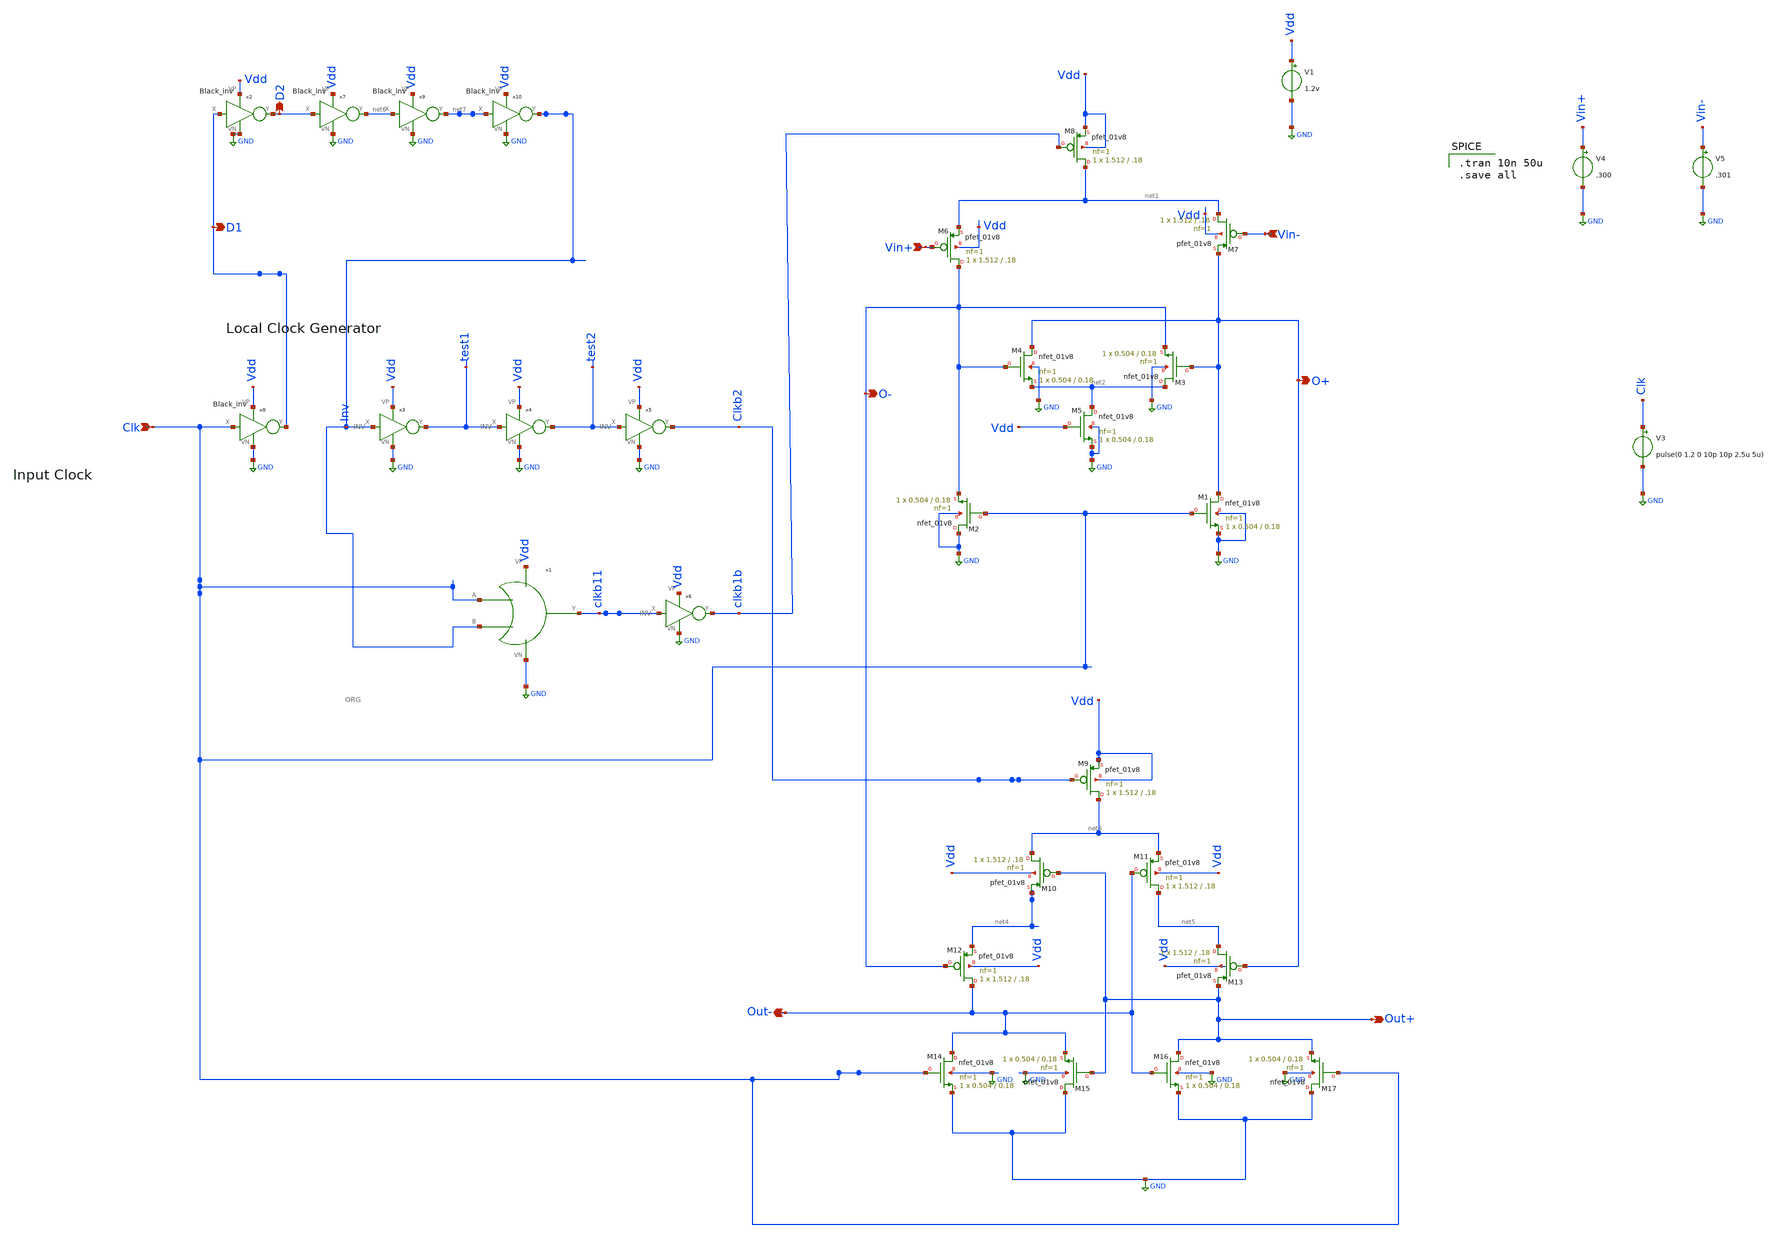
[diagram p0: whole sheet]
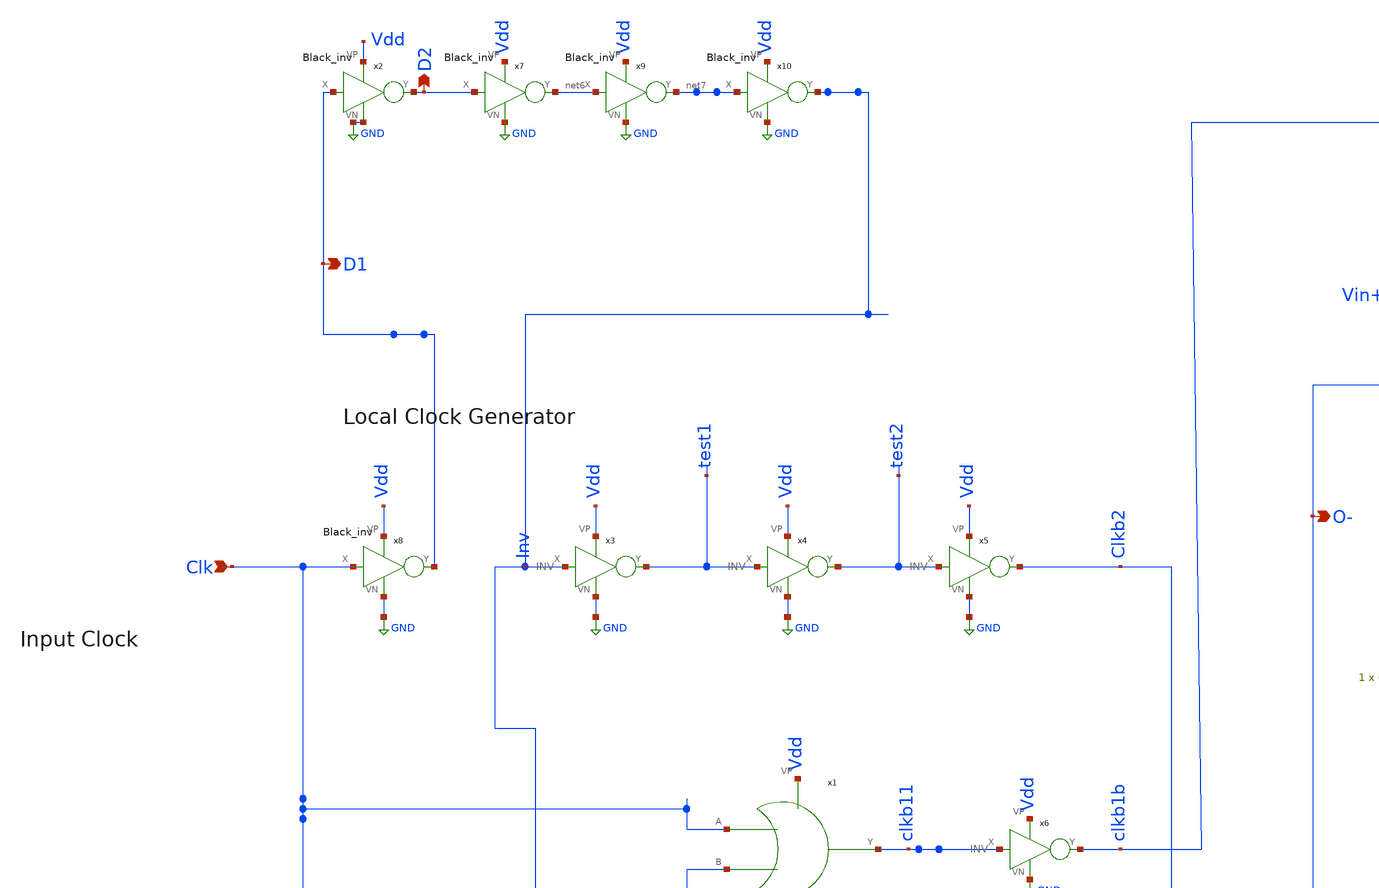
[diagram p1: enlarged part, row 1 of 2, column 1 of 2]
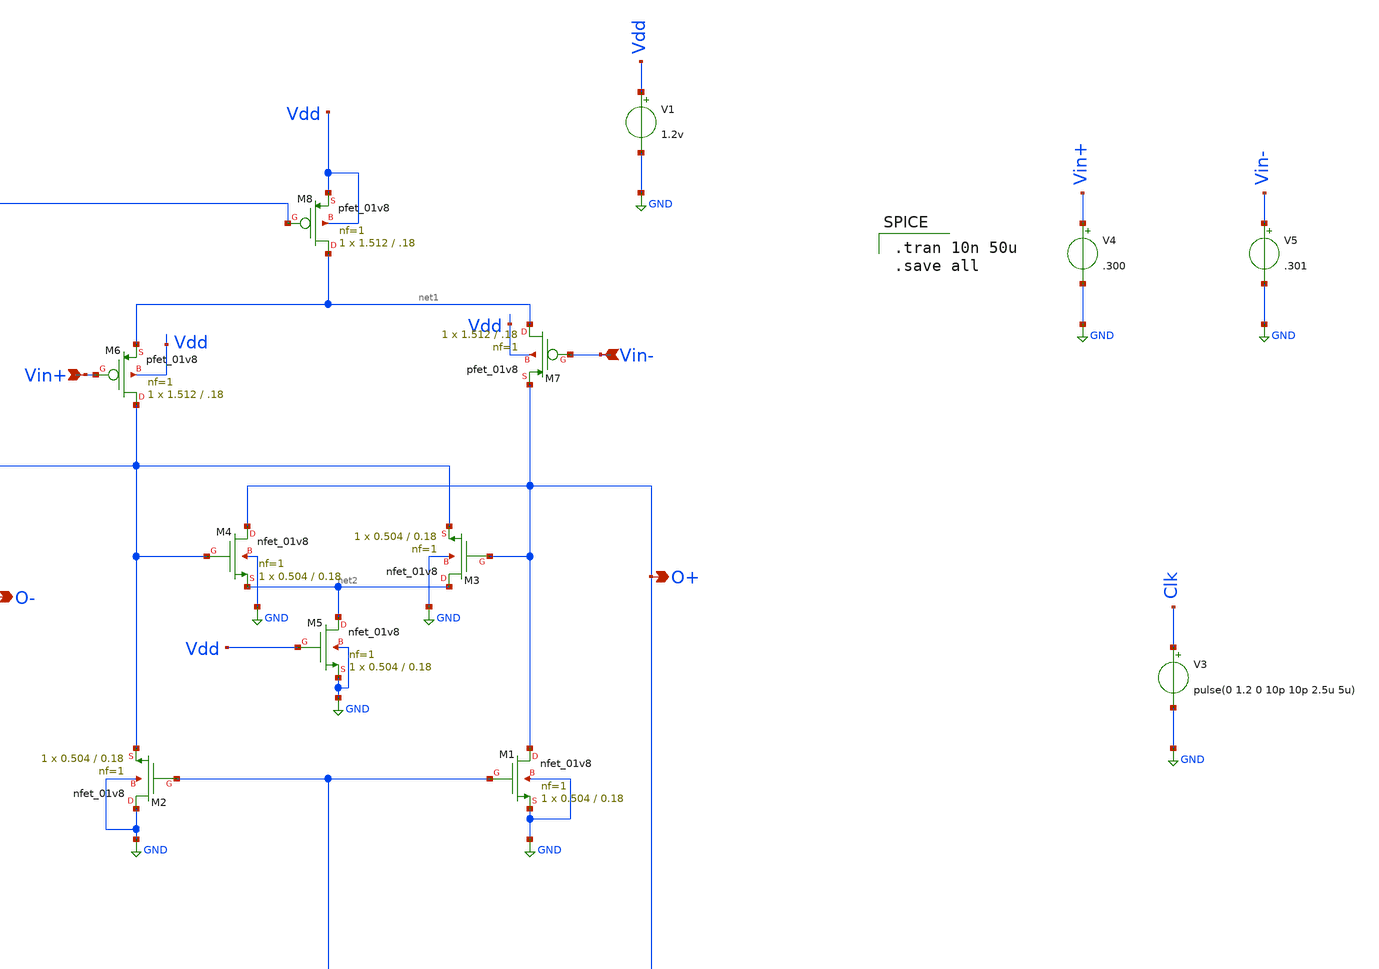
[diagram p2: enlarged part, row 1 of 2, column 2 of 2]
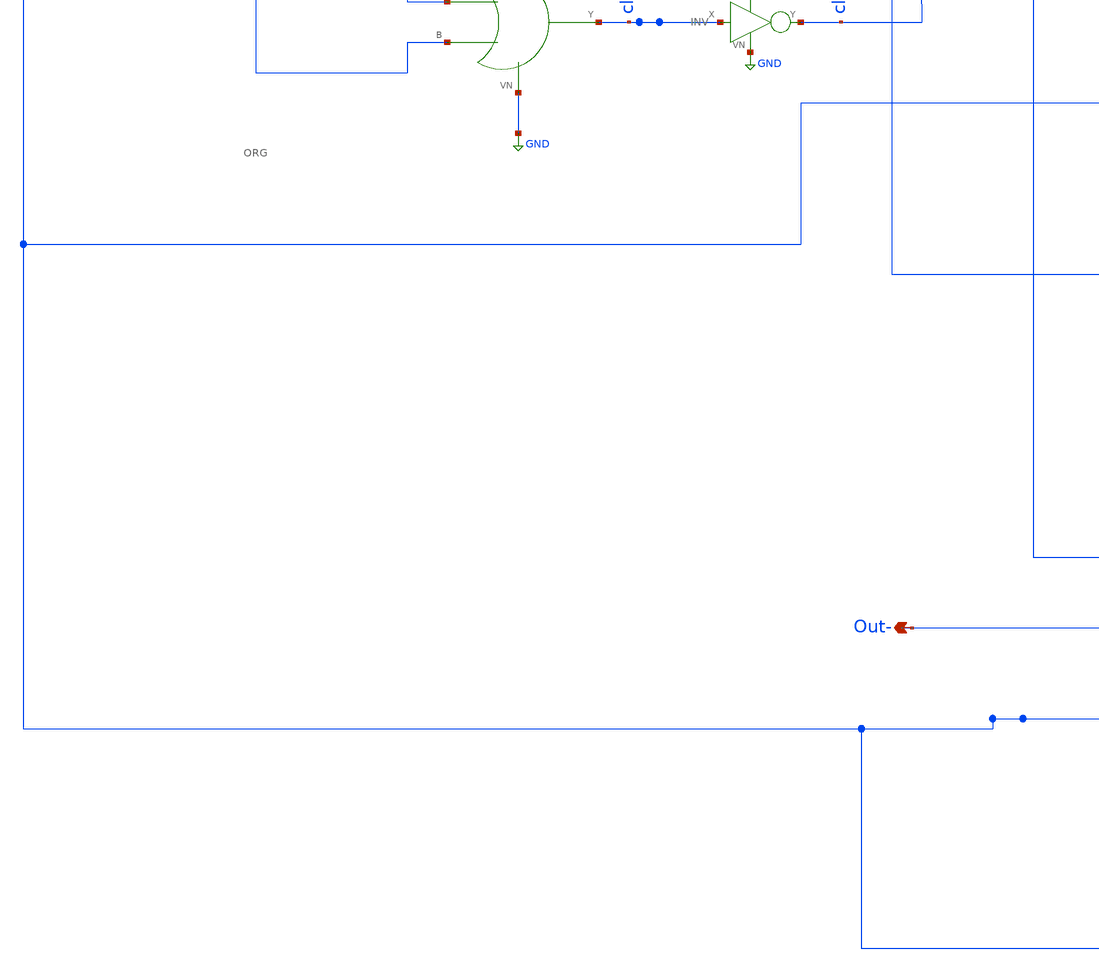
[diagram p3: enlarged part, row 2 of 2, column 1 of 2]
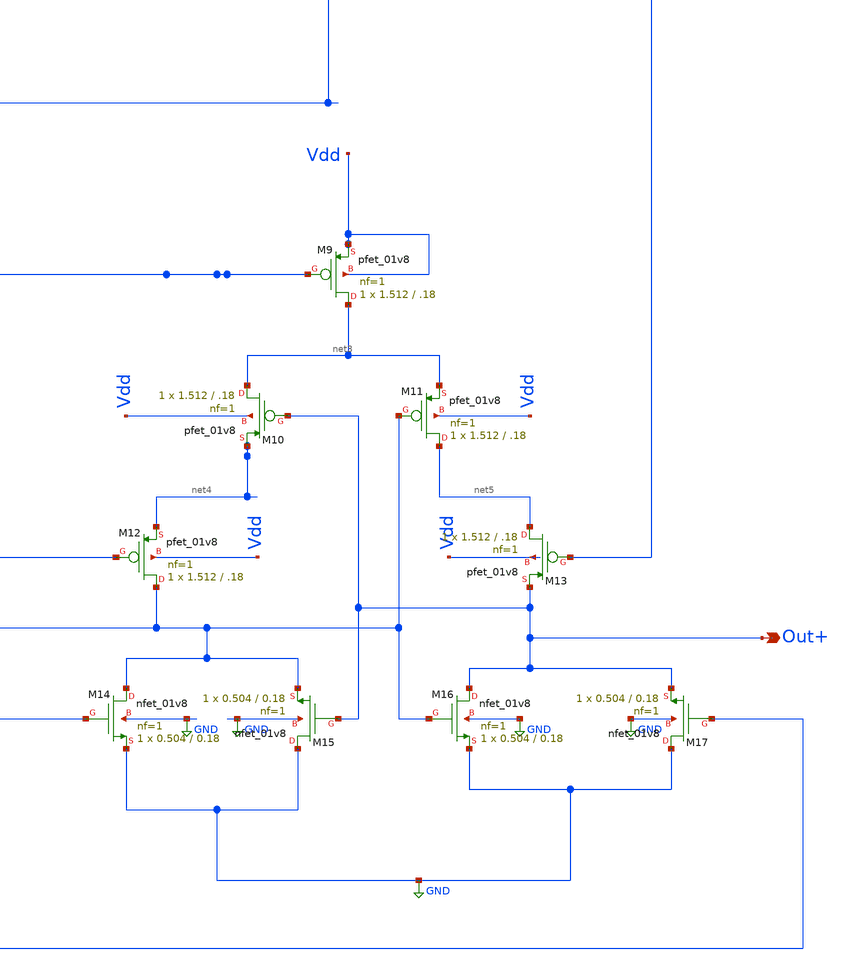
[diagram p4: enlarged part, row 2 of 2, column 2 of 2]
** sch_path: Blocks/Comparator/Comparator.sch
**.subckt Comparator Vin+ Vin- Clk Out+ Out- D2 D1 O- O+
*.ipin Vin+
*.ipin Vin-
*.ipin Clk
*.opin Out+
*.opin Out-
*.opin D2
*.opin D1
*.opin O-
*.opin O+
XM8 net1 clkb1b Vdd Vdd sky130_fd_pr__pfet_01v8 L=.18 W=1.512 nf=1 ad='int((nf+1)/2) * W/nf * 0.29' as='int((nf+2)/2) * W/nf * 0.29'
+ pd='2*int((nf+1)/2) * (W/nf + 0.29)' ps='2*int((nf+2)/2) * (W/nf + 0.29)' nrd='0.29 / W' nrs='0.29 / W'
+ sa=0 sb=0 sd=0 mult=1 m=1
x1 Inv Clk clkb11 Vdd GND ORG
x3 Inv test1 Vdd GND INV
x4 test1 test2 Vdd GND INV
x5 test2 Clkb2 Vdd GND INV
x6 clkb11 clkb1b Vdd GND INV
XM4 O+ O- net2 GND sky130_fd_pr__nfet_01v8 L=0.18 W=0.504 nf=1 ad='int((nf+1)/2) * W/nf * 0.29' as='int((nf+2)/2) * W/nf * 0.29'
+ pd='2*int((nf+1)/2) * (W/nf + 0.29)' ps='2*int((nf+2)/2) * (W/nf + 0.29)' nrd='0.29 / W' nrs='0.29 / W'
+ sa=0 sb=0 sd=0 mult=1 m=1
XM6 O- Vin+ net1 Vdd sky130_fd_pr__pfet_01v8 L=.18 W=1.512 nf=1 ad='int((nf+1)/2) * W/nf * 0.29' as='int((nf+2)/2) * W/nf * 0.29'
+ pd='2*int((nf+1)/2) * (W/nf + 0.29)' ps='2*int((nf+2)/2) * (W/nf + 0.29)' nrd='0.29 / W' nrs='0.29 / W'
+ sa=0 sb=0 sd=0 mult=1 m=1
XM7 net1 Vin- O+ Vdd sky130_fd_pr__pfet_01v8 L=.18 W=1.512 nf=1 ad='int((nf+1)/2) * W/nf * 0.29' as='int((nf+2)/2) * W/nf * 0.29'
+ pd='2*int((nf+1)/2) * (W/nf + 0.29)' ps='2*int((nf+2)/2) * (W/nf + 0.29)' nrd='0.29 / W' nrs='0.29 / W'
+ sa=0 sb=0 sd=0 mult=1 m=1
XM3 net2 O+ O- GND sky130_fd_pr__nfet_01v8 L=0.18 W=0.504 nf=1 ad='int((nf+1)/2) * W/nf * 0.29' as='int((nf+2)/2) * W/nf * 0.29'
+ pd='2*int((nf+1)/2) * (W/nf + 0.29)' ps='2*int((nf+2)/2) * (W/nf + 0.29)' nrd='0.29 / W' nrs='0.29 / W'
+ sa=0 sb=0 sd=0 mult=1 m=1
XM5 net2 Vdd GND GND sky130_fd_pr__nfet_01v8 L=0.18 W=0.504 nf=1 ad='int((nf+1)/2) * W/nf * 0.29' as='int((nf+2)/2) * W/nf * 0.29'
+ pd='2*int((nf+1)/2) * (W/nf + 0.29)' ps='2*int((nf+2)/2) * (W/nf + 0.29)' nrd='0.29 / W' nrs='0.29 / W'
+ sa=0 sb=0 sd=0 mult=1 m=1
XM2 GND Clk O- GND sky130_fd_pr__nfet_01v8 L=0.18 W=0.504 nf=1 ad='int((nf+1)/2) * W/nf * 0.29' as='int((nf+2)/2) * W/nf * 0.29'
+ pd='2*int((nf+1)/2) * (W/nf + 0.29)' ps='2*int((nf+2)/2) * (W/nf + 0.29)' nrd='0.29 / W' nrs='0.29 / W'
+ sa=0 sb=0 sd=0 mult=1 m=1
XM1 O+ Clk GND GND sky130_fd_pr__nfet_01v8 L=0.18 W=0.504 nf=1 ad='int((nf+1)/2) * W/nf * 0.29' as='int((nf+2)/2) * W/nf * 0.29'
+ pd='2*int((nf+1)/2) * (W/nf + 0.29)' ps='2*int((nf+2)/2) * (W/nf + 0.29)' nrd='0.29 / W' nrs='0.29 / W'
+ sa=0 sb=0 sd=0 mult=1 m=1
XM14 Out- Clk GND GND sky130_fd_pr__nfet_01v8 L=0.18 W=0.504 nf=1 ad='int((nf+1)/2) * W/nf * 0.29' as='int((nf+2)/2) * W/nf * 0.29'
+ pd='2*int((nf+1)/2) * (W/nf + 0.29)' ps='2*int((nf+2)/2) * (W/nf + 0.29)' nrd='0.29 / W' nrs='0.29 / W'
+ sa=0 sb=0 sd=0 mult=1 m=1
XM15 GND Out+ Out- GND sky130_fd_pr__nfet_01v8 L=0.18 W=0.504 nf=1 ad='int((nf+1)/2) * W/nf * 0.29' as='int((nf+2)/2) * W/nf * 0.29'
+ pd='2*int((nf+1)/2) * (W/nf + 0.29)' ps='2*int((nf+2)/2) * (W/nf + 0.29)' nrd='0.29 / W' nrs='0.29 / W'
+ sa=0 sb=0 sd=0 mult=1 m=1
XM16 Out+ Out- GND GND sky130_fd_pr__nfet_01v8 L=0.18 W=0.504 nf=1 ad='int((nf+1)/2) * W/nf * 0.29' as='int((nf+2)/2) * W/nf * 0.29'
+ pd='2*int((nf+1)/2) * (W/nf + 0.29)' ps='2*int((nf+2)/2) * (W/nf + 0.29)' nrd='0.29 / W' nrs='0.29 / W'
+ sa=0 sb=0 sd=0 mult=1 m=1
XM17 GND Clk Out+ GND sky130_fd_pr__nfet_01v8 L=0.18 W=0.504 nf=1 ad='int((nf+1)/2) * W/nf * 0.29' as='int((nf+2)/2) * W/nf * 0.29'
+ pd='2*int((nf+1)/2) * (W/nf + 0.29)' ps='2*int((nf+2)/2) * (W/nf + 0.29)' nrd='0.29 / W' nrs='0.29 / W'
+ sa=0 sb=0 sd=0 mult=1 m=1
XM9 net3 Clkb2 Vdd Vdd sky130_fd_pr__pfet_01v8 L=.18 W=1.512 nf=1 ad='int((nf+1)/2) * W/nf * 0.29' as='int((nf+2)/2) * W/nf * 0.29'
+ pd='2*int((nf+1)/2) * (W/nf + 0.29)' ps='2*int((nf+2)/2) * (W/nf + 0.29)' nrd='0.29 / W' nrs='0.29 / W'
+ sa=0 sb=0 sd=0 mult=1 m=1
XM10 net3 Out+ net4 Vdd sky130_fd_pr__pfet_01v8 L=.18 W=1.512 nf=1 ad='int((nf+1)/2) * W/nf * 0.29' as='int((nf+2)/2) * W/nf * 0.29'
+ pd='2*int((nf+1)/2) * (W/nf + 0.29)' ps='2*int((nf+2)/2) * (W/nf + 0.29)' nrd='0.29 / W' nrs='0.29 / W'
+ sa=0 sb=0 sd=0 mult=1 m=1
XM11 net5 Out- net3 Vdd sky130_fd_pr__pfet_01v8 L=.18 W=1.512 nf=1 ad='int((nf+1)/2) * W/nf * 0.29' as='int((nf+2)/2) * W/nf * 0.29'
+ pd='2*int((nf+1)/2) * (W/nf + 0.29)' ps='2*int((nf+2)/2) * (W/nf + 0.29)' nrd='0.29 / W' nrs='0.29 / W'
+ sa=0 sb=0 sd=0 mult=1 m=1
XM13 net5 O+ Out+ Vdd sky130_fd_pr__pfet_01v8 L=.18 W=1.512 nf=1 ad='int((nf+1)/2) * W/nf * 0.29' as='int((nf+2)/2) * W/nf * 0.29'
+ pd='2*int((nf+1)/2) * (W/nf + 0.29)' ps='2*int((nf+2)/2) * (W/nf + 0.29)' nrd='0.29 / W' nrs='0.29 / W'
+ sa=0 sb=0 sd=0 mult=1 m=1
XM12 Out- O- net4 Vdd sky130_fd_pr__pfet_01v8 L=.18 W=1.512 nf=1 ad='int((nf+1)/2) * W/nf * 0.29' as='int((nf+2)/2) * W/nf * 0.29'
+ pd='2*int((nf+1)/2) * (W/nf + 0.29)' ps='2*int((nf+2)/2) * (W/nf + 0.29)' nrd='0.29 / W' nrs='0.29 / W'
+ sa=0 sb=0 sd=0 mult=1 m=1
V1 Vdd GND 1.2v
V4 Vin+ GND .300
V5 Vin- GND .301
x7 D2 net6 Vdd GND black_inv
x8 Clk D1 Vdd GND black_inv
x2 D1 D2 Vdd GND black_inv
V3 Clk GND pulse(0 1.2 0 10p 10p 2.5u 5u)
x9 net6 net7 Vdd GND black_inv
x10 net7 Inv Vdd GND black_inv
**** begin user architecture code

.tran 10n 50u
.save all


** opencircuitdesign pdks install
.lib $::SKYWATER_MODELS/sky130.lib.spice tt


**** end user architecture code
**.ends

* expanding   symbol:  pico/akshat_comp/ezyzip/PICO/OR_gate/ORG.sym # of pins=5
** sym_path: component/OR_gate/ORG.sym
** sch_path: component/OR_gate/ORG.sch
.subckt ORG B A Y VP VN
*.ipin A
*.ipin B
*.opin Y
*.iopin VP
*.iopin VN
XM3 Y A VN VN sky130_fd_pr__nfet_01v8 L=0.18 W=0.504 nf=1 ad='int((nf+1)/2) * W/nf * 0.29' as='int((nf+2)/2) * W/nf * 0.29'
+ pd='2*int((nf+1)/2) * (W/nf + 0.29)' ps='2*int((nf+2)/2) * (W/nf + 0.29)' nrd='0.29 / W' nrs='0.29 / W'
+ sa=0 sb=0 sd=0 mult=1 m=1
XM8 net1 A VP VP sky130_fd_pr__pfet_01v8 L=.18 W=1.512 nf=1 ad='int((nf+1)/2) * W/nf * 0.29' as='int((nf+2)/2) * W/nf * 0.29'
+ pd='2*int((nf+1)/2) * (W/nf + 0.29)' ps='2*int((nf+2)/2) * (W/nf + 0.29)' nrd='0.29 / W' nrs='0.29 / W'
+ sa=0 sb=0 sd=0 mult=1 m=1
XM2 Y B net1 VP sky130_fd_pr__pfet_01v8 L=.18 W=1.512 nf=1 ad='int((nf+1)/2) * W/nf * 0.29' as='int((nf+2)/2) * W/nf * 0.29'
+ pd='2*int((nf+1)/2) * (W/nf + 0.29)' ps='2*int((nf+2)/2) * (W/nf + 0.29)' nrd='0.29 / W' nrs='0.29 / W'
+ sa=0 sb=0 sd=0 mult=1 m=1
XM1 Y B VN VN sky130_fd_pr__nfet_01v8 L=0.18 W=0.504 nf=1 ad='int((nf+1)/2) * W/nf * 0.29' as='int((nf+2)/2) * W/nf * 0.29'
+ pd='2*int((nf+1)/2) * (W/nf + 0.29)' ps='2*int((nf+2)/2) * (W/nf + 0.29)' nrd='0.29 / W' nrs='0.29 / W'
+ sa=0 sb=0 sd=0 mult=1 m=1
.ends


* expanding   symbol:  pico/akshat_comp/ezyzip/PICO/Inverter/INV.sym # of pins=4
** sym_path: component/Inverter/INV.sym
** sch_path: component/Inverter/INV.sch
.subckt INV X Y VP VN
*.ipin X
*.opin Y
*.iopin VN
*.iopin VP
XM8 Y X VP VP sky130_fd_pr__pfet_01v8 L=.18 W=1.512 nf=1 ad='int((nf+1)/2) * W/nf * 0.29' as='int((nf+2)/2) * W/nf * 0.29'
+ pd='2*int((nf+1)/2) * (W/nf + 0.29)' ps='2*int((nf+2)/2) * (W/nf + 0.29)' nrd='0.29 / W' nrs='0.29 / W'
+ sa=0 sb=0 sd=0 mult=1 m=1
XM4 Y X VN VN sky130_fd_pr__nfet_01v8 L=0.18 W=0.42 nf=1 ad='int((nf+1)/2) * W/nf * 0.29' as='int((nf+2)/2) * W/nf * 0.29'
+ pd='2*int((nf+1)/2) * (W/nf + 0.29)' ps='2*int((nf+2)/2) * (W/nf + 0.29)' nrd='0.29 / W' nrs='0.29 / W'
+ sa=0 sb=0 sd=0 mult=1 m=1
.ends


* expanding   symbol:  pico/akshat_comp/ezyzip/PICO/black_inv_1/black_inv.sym # of pins=4
** sym_path: component/black_inv_1/black_inv.sym
** sch_path: component/black_inv_1/black_inv.sch
.subckt black_inv X Y VP VN
*.ipin X
*.opin Y
*.iopin VN
*.iopin VP
XM8 Y X VP VP sky130_fd_pr__pfet_01v8 L=.18 W=1.59 nf=1 ad='int((nf+1)/2) * W/nf * 0.29' as='int((nf+2)/2) * W/nf * 0.29'
+ pd='2*int((nf+1)/2) * (W/nf + 0.29)' ps='2*int((nf+2)/2) * (W/nf + 0.29)' nrd='0.29 / W' nrs='0.29 / W'
+ sa=0 sb=0 sd=0 mult=1 m=1
XM4 Y X VN VN sky130_fd_pr__nfet_01v8 L=0.18 W=0.502 nf=1 ad='int((nf+1)/2) * W/nf * 0.29' as='int((nf+2)/2) * W/nf * 0.29'
+ pd='2*int((nf+1)/2) * (W/nf + 0.29)' ps='2*int((nf+2)/2) * (W/nf + 0.29)' nrd='0.29 / W' nrs='0.29 / W'
+ sa=0 sb=0 sd=0 mult=1 m=1
.ends

.GLOBAL GND
.end
